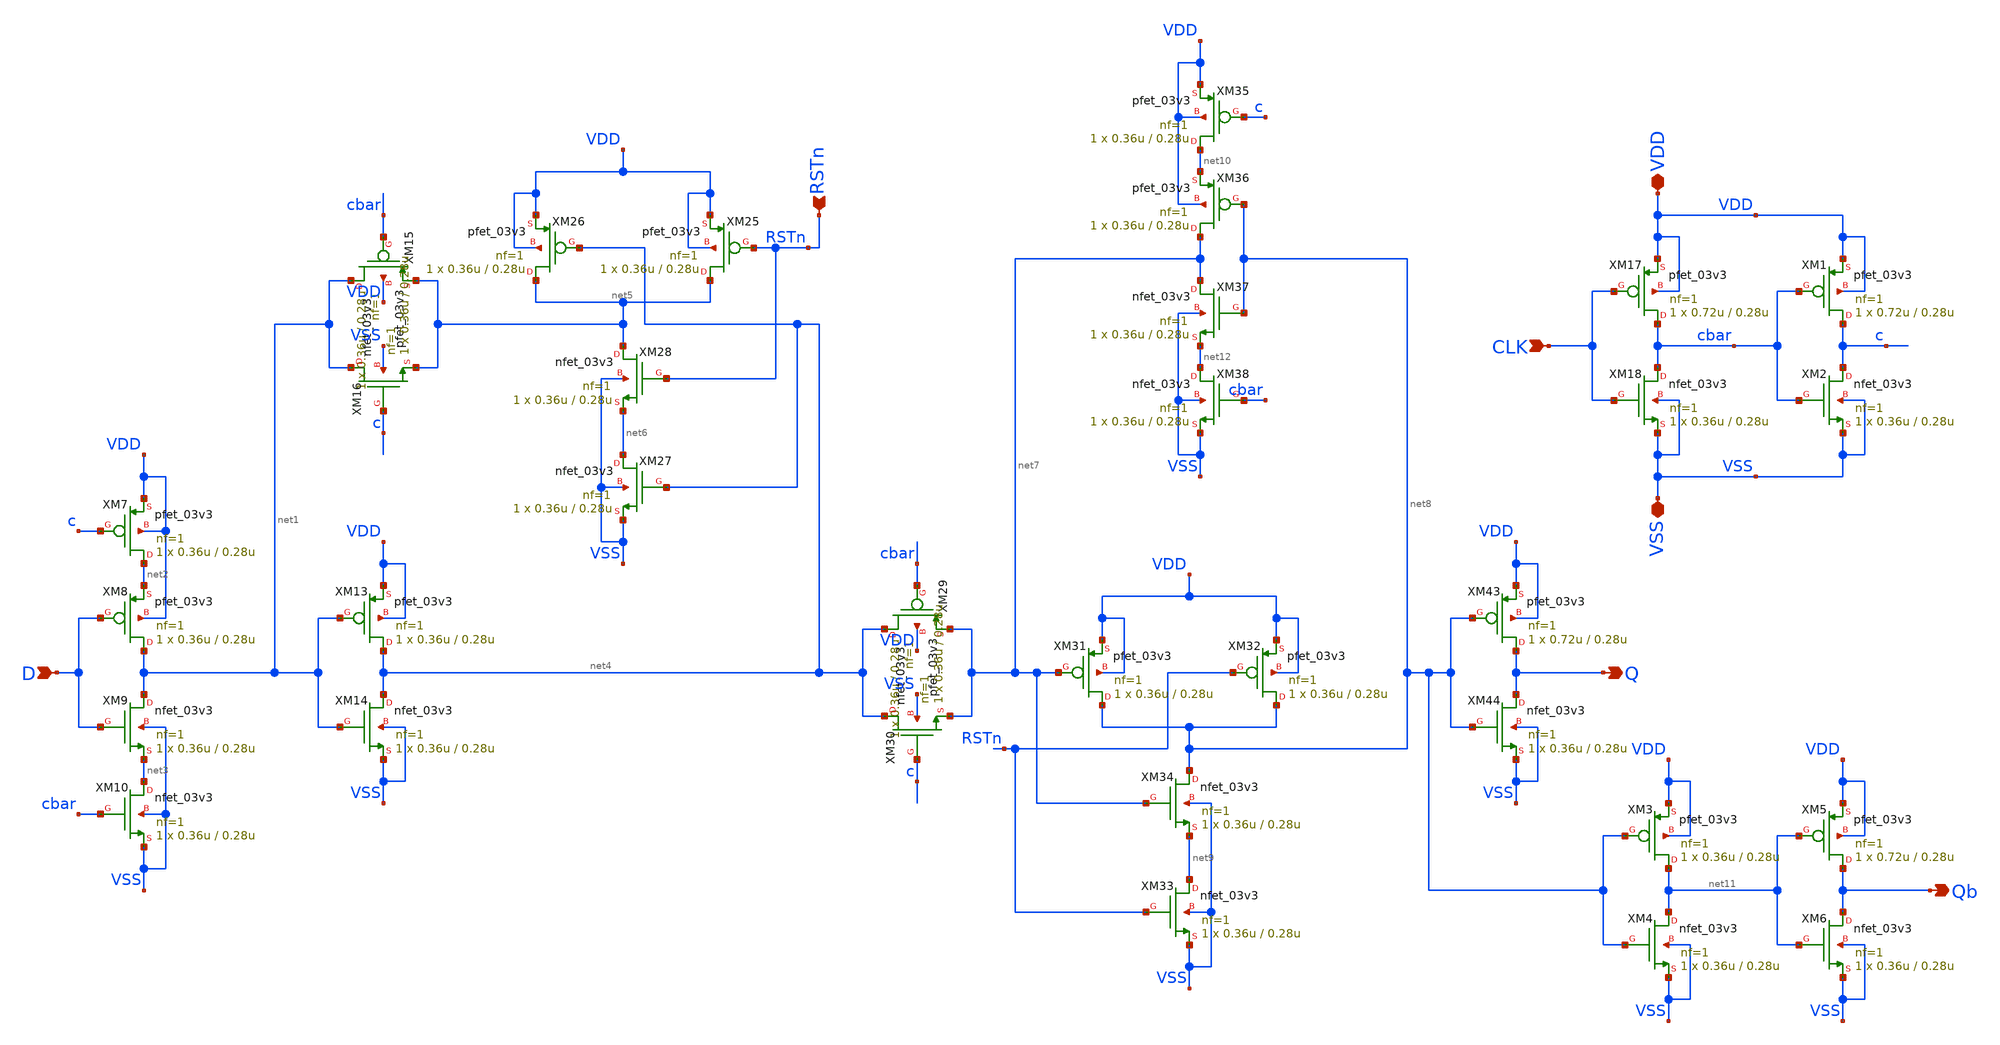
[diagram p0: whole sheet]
** sch_path: CAD6/cad2_dff.sch
**.subckt cad2_dff D CLK Q VDD VSS RSTn Qb
*.ipin D
*.ipin CLK
*.opin Q
*.iopin VDD
*.iopin VSS
*.ipin RSTn
*.opin Qb
XM7 net2 c VDD VDD pfet_03v3 L=0.28u W=0.36u nf=1 ad='int((nf+1)/2) * W/nf * 0.18u' as='int((nf+2)/2) * W/nf * 0.18u'
+ pd='2*int((nf+1)/2) * (W/nf + 0.18u)' ps='2*int((nf+2)/2) * (W/nf + 0.18u)' nrd='0.18u / W' nrs='0.18u / W'
+ sa=0 sb=0 sd=0 m=1
XM8 net1 D net2 VDD pfet_03v3 L=0.28u W=0.36u nf=1 ad='int((nf+1)/2) * W/nf * 0.18u' as='int((nf+2)/2) * W/nf * 0.18u'
+ pd='2*int((nf+1)/2) * (W/nf + 0.18u)' ps='2*int((nf+2)/2) * (W/nf + 0.18u)' nrd='0.18u / W' nrs='0.18u / W'
+ sa=0 sb=0 sd=0 m=1
XM9 net1 D net3 VSS nfet_03v3 L=0.28u W=0.36u nf=1 ad='int((nf+1)/2) * W/nf * 0.18u' as='int((nf+2)/2) * W/nf * 0.18u'
+ pd='2*int((nf+1)/2) * (W/nf + 0.18u)' ps='2*int((nf+2)/2) * (W/nf + 0.18u)' nrd='0.18u / W' nrs='0.18u / W'
+ sa=0 sb=0 sd=0 m=1
XM10 net3 cbar VSS VSS nfet_03v3 L=0.28u W=0.36u nf=1 ad='int((nf+1)/2) * W/nf * 0.18u' as='int((nf+2)/2) * W/nf * 0.18u'
+ pd='2*int((nf+1)/2) * (W/nf + 0.18u)' ps='2*int((nf+2)/2) * (W/nf + 0.18u)' nrd='0.18u / W' nrs='0.18u / W'
+ sa=0 sb=0 sd=0 m=1
XM13 net4 net1 VDD VDD pfet_03v3 L=0.28u W=0.36u nf=1 ad='int((nf+1)/2) * W/nf * 0.18u' as='int((nf+2)/2) * W/nf * 0.18u'
+ pd='2*int((nf+1)/2) * (W/nf + 0.18u)' ps='2*int((nf+2)/2) * (W/nf + 0.18u)' nrd='0.18u / W' nrs='0.18u / W'
+ sa=0 sb=0 sd=0 m=1
XM14 net4 net1 VSS VSS nfet_03v3 L=0.28u W=0.36u nf=1 ad='int((nf+1)/2) * W/nf * 0.18u' as='int((nf+2)/2) * W/nf * 0.18u'
+ pd='2*int((nf+1)/2) * (W/nf + 0.18u)' ps='2*int((nf+2)/2) * (W/nf + 0.18u)' nrd='0.18u / W' nrs='0.18u / W'
+ sa=0 sb=0 sd=0 m=1
XM15 net1 cbar net5 VDD pfet_03v3 L=0.28u W=0.36u nf=1 ad='int((nf+1)/2) * W/nf * 0.18u' as='int((nf+2)/2) * W/nf * 0.18u'
+ pd='2*int((nf+1)/2) * (W/nf + 0.18u)' ps='2*int((nf+2)/2) * (W/nf + 0.18u)' nrd='0.18u / W' nrs='0.18u / W'
+ sa=0 sb=0 sd=0 m=1
XM16 net1 c net5 VSS nfet_03v3 L=0.28u W=0.36u nf=1 ad='int((nf+1)/2) * W/nf * 0.18u' as='int((nf+2)/2) * W/nf * 0.18u'
+ pd='2*int((nf+1)/2) * (W/nf + 0.18u)' ps='2*int((nf+2)/2) * (W/nf + 0.18u)' nrd='0.18u / W' nrs='0.18u / W'
+ sa=0 sb=0 sd=0 m=1
XM17 cbar CLK VDD VDD pfet_03v3 L=0.28u W=0.72u nf=1 ad='int((nf+1)/2) * W/nf * 0.18u' as='int((nf+2)/2) * W/nf * 0.18u'
+ pd='2*int((nf+1)/2) * (W/nf + 0.18u)' ps='2*int((nf+2)/2) * (W/nf + 0.18u)' nrd='0.18u / W' nrs='0.18u / W'
+ sa=0 sb=0 sd=0 m=1
XM18 cbar CLK VSS VSS nfet_03v3 L=0.28u W=0.36u nf=1 ad='int((nf+1)/2) * W/nf * 0.18u' as='int((nf+2)/2) * W/nf * 0.18u'
+ pd='2*int((nf+1)/2) * (W/nf + 0.18u)' ps='2*int((nf+2)/2) * (W/nf + 0.18u)' nrd='0.18u / W' nrs='0.18u / W'
+ sa=0 sb=0 sd=0 m=1
XM25 net5 RSTn VDD VDD pfet_03v3 L=0.28u W=0.36u nf=1 ad='int((nf+1)/2) * W/nf * 0.18u' as='int((nf+2)/2) * W/nf * 0.18u'
+ pd='2*int((nf+1)/2) * (W/nf + 0.18u)' ps='2*int((nf+2)/2) * (W/nf + 0.18u)' nrd='0.18u / W' nrs='0.18u / W'
+ sa=0 sb=0 sd=0 m=1
XM26 net5 net4 VDD VDD pfet_03v3 L=0.28u W=0.36u nf=1 ad='int((nf+1)/2) * W/nf * 0.18u' as='int((nf+2)/2) * W/nf * 0.18u'
+ pd='2*int((nf+1)/2) * (W/nf + 0.18u)' ps='2*int((nf+2)/2) * (W/nf + 0.18u)' nrd='0.18u / W' nrs='0.18u / W'
+ sa=0 sb=0 sd=0 m=1
XM27 net6 net4 VSS VSS nfet_03v3 L=0.28u W=0.36u nf=1 ad='int((nf+1)/2) * W/nf * 0.18u' as='int((nf+2)/2) * W/nf * 0.18u'
+ pd='2*int((nf+1)/2) * (W/nf + 0.18u)' ps='2*int((nf+2)/2) * (W/nf + 0.18u)' nrd='0.18u / W' nrs='0.18u / W'
+ sa=0 sb=0 sd=0 m=1
XM28 net5 RSTn net6 VSS nfet_03v3 L=0.28u W=0.36u nf=1 ad='int((nf+1)/2) * W/nf * 0.18u' as='int((nf+2)/2) * W/nf * 0.18u'
+ pd='2*int((nf+1)/2) * (W/nf + 0.18u)' ps='2*int((nf+2)/2) * (W/nf + 0.18u)' nrd='0.18u / W' nrs='0.18u / W'
+ sa=0 sb=0 sd=0 m=1
XM29 net4 cbar net7 VDD pfet_03v3 L=0.28u W=0.36u nf=1 ad='int((nf+1)/2) * W/nf * 0.18u' as='int((nf+2)/2) * W/nf * 0.18u'
+ pd='2*int((nf+1)/2) * (W/nf + 0.18u)' ps='2*int((nf+2)/2) * (W/nf + 0.18u)' nrd='0.18u / W' nrs='0.18u / W'
+ sa=0 sb=0 sd=0 m=1
XM30 net4 c net7 VSS nfet_03v3 L=0.28u W=0.36u nf=1 ad='int((nf+1)/2) * W/nf * 0.18u' as='int((nf+2)/2) * W/nf * 0.18u'
+ pd='2*int((nf+1)/2) * (W/nf + 0.18u)' ps='2*int((nf+2)/2) * (W/nf + 0.18u)' nrd='0.18u / W' nrs='0.18u / W'
+ sa=0 sb=0 sd=0 m=1
XM31 net8 net7 VDD VDD pfet_03v3 L=0.28u W=0.36u nf=1 ad='int((nf+1)/2) * W/nf * 0.18u' as='int((nf+2)/2) * W/nf * 0.18u'
+ pd='2*int((nf+1)/2) * (W/nf + 0.18u)' ps='2*int((nf+2)/2) * (W/nf + 0.18u)' nrd='0.18u / W' nrs='0.18u / W'
+ sa=0 sb=0 sd=0 m=1
XM32 net8 RSTn VDD VDD pfet_03v3 L=0.28u W=0.36u nf=1 ad='int((nf+1)/2) * W/nf * 0.18u' as='int((nf+2)/2) * W/nf * 0.18u'
+ pd='2*int((nf+1)/2) * (W/nf + 0.18u)' ps='2*int((nf+2)/2) * (W/nf + 0.18u)' nrd='0.18u / W' nrs='0.18u / W'
+ sa=0 sb=0 sd=0 m=1
XM33 net9 RSTn VSS VSS nfet_03v3 L=0.28u W=0.36u nf=1 ad='int((nf+1)/2) * W/nf * 0.18u' as='int((nf+2)/2) * W/nf * 0.18u'
+ pd='2*int((nf+1)/2) * (W/nf + 0.18u)' ps='2*int((nf+2)/2) * (W/nf + 0.18u)' nrd='0.18u / W' nrs='0.18u / W'
+ sa=0 sb=0 sd=0 m=1
XM34 net8 net7 net9 VSS nfet_03v3 L=0.28u W=0.36u nf=1 ad='int((nf+1)/2) * W/nf * 0.18u' as='int((nf+2)/2) * W/nf * 0.18u'
+ pd='2*int((nf+1)/2) * (W/nf + 0.18u)' ps='2*int((nf+2)/2) * (W/nf + 0.18u)' nrd='0.18u / W' nrs='0.18u / W'
+ sa=0 sb=0 sd=0 m=1
XM35 net10 c VDD VDD pfet_03v3 L=0.28u W=0.36u nf=1 ad='int((nf+1)/2) * W/nf * 0.18u' as='int((nf+2)/2) * W/nf * 0.18u'
+ pd='2*int((nf+1)/2) * (W/nf + 0.18u)' ps='2*int((nf+2)/2) * (W/nf + 0.18u)' nrd='0.18u / W' nrs='0.18u / W'
+ sa=0 sb=0 sd=0 m=1
XM36 net7 net8 net10 VDD pfet_03v3 L=0.28u W=0.36u nf=1 ad='int((nf+1)/2) * W/nf * 0.18u' as='int((nf+2)/2) * W/nf * 0.18u'
+ pd='2*int((nf+1)/2) * (W/nf + 0.18u)' ps='2*int((nf+2)/2) * (W/nf + 0.18u)' nrd='0.18u / W' nrs='0.18u / W'
+ sa=0 sb=0 sd=0 m=1
XM37 net7 net8 net12 VSS nfet_03v3 L=0.28u W=0.36u nf=1 ad='int((nf+1)/2) * W/nf * 0.18u' as='int((nf+2)/2) * W/nf * 0.18u'
+ pd='2*int((nf+1)/2) * (W/nf + 0.18u)' ps='2*int((nf+2)/2) * (W/nf + 0.18u)' nrd='0.18u / W' nrs='0.18u / W'
+ sa=0 sb=0 sd=0 m=1
XM38 net12 cbar VSS VSS nfet_03v3 L=0.28u W=0.36u nf=1 ad='int((nf+1)/2) * W/nf * 0.18u' as='int((nf+2)/2) * W/nf * 0.18u'
+ pd='2*int((nf+1)/2) * (W/nf + 0.18u)' ps='2*int((nf+2)/2) * (W/nf + 0.18u)' nrd='0.18u / W' nrs='0.18u / W'
+ sa=0 sb=0 sd=0 m=1
XM43 Q net8 VDD VDD pfet_03v3 L=0.28u W=0.72u nf=1 ad='int((nf+1)/2) * W/nf * 0.18u' as='int((nf+2)/2) * W/nf * 0.18u'
+ pd='2*int((nf+1)/2) * (W/nf + 0.18u)' ps='2*int((nf+2)/2) * (W/nf + 0.18u)' nrd='0.18u / W' nrs='0.18u / W'
+ sa=0 sb=0 sd=0 m=1
XM44 Q net8 VSS VSS nfet_03v3 L=0.28u W=0.36u nf=1 ad='int((nf+1)/2) * W/nf * 0.18u' as='int((nf+2)/2) * W/nf * 0.18u'
+ pd='2*int((nf+1)/2) * (W/nf + 0.18u)' ps='2*int((nf+2)/2) * (W/nf + 0.18u)' nrd='0.18u / W' nrs='0.18u / W'
+ sa=0 sb=0 sd=0 m=1
XM1 c cbar VDD VDD pfet_03v3 L=0.28u W=0.72u nf=1 ad='int((nf+1)/2) * W/nf * 0.18u' as='int((nf+2)/2) * W/nf * 0.18u'
+ pd='2*int((nf+1)/2) * (W/nf + 0.18u)' ps='2*int((nf+2)/2) * (W/nf + 0.18u)' nrd='0.18u / W' nrs='0.18u / W'
+ sa=0 sb=0 sd=0 m=1
XM2 c cbar VSS VSS nfet_03v3 L=0.28u W=0.36u nf=1 ad='int((nf+1)/2) * W/nf * 0.18u' as='int((nf+2)/2) * W/nf * 0.18u'
+ pd='2*int((nf+1)/2) * (W/nf + 0.18u)' ps='2*int((nf+2)/2) * (W/nf + 0.18u)' nrd='0.18u / W' nrs='0.18u / W'
+ sa=0 sb=0 sd=0 m=1
XM3 net11 net8 VDD VDD pfet_03v3 L=0.28u W=0.36u nf=1 ad='int((nf+1)/2) * W/nf * 0.18u' as='int((nf+2)/2) * W/nf * 0.18u'
+ pd='2*int((nf+1)/2) * (W/nf + 0.18u)' ps='2*int((nf+2)/2) * (W/nf + 0.18u)' nrd='0.18u / W' nrs='0.18u / W'
+ sa=0 sb=0 sd=0 m=1
XM4 net11 net8 VSS VSS nfet_03v3 L=0.28u W=0.36u nf=1 ad='int((nf+1)/2) * W/nf * 0.18u' as='int((nf+2)/2) * W/nf * 0.18u'
+ pd='2*int((nf+1)/2) * (W/nf + 0.18u)' ps='2*int((nf+2)/2) * (W/nf + 0.18u)' nrd='0.18u / W' nrs='0.18u / W'
+ sa=0 sb=0 sd=0 m=1
XM5 Qb net11 VDD VDD pfet_03v3 L=0.28u W=0.72u nf=1 ad='int((nf+1)/2) * W/nf * 0.18u' as='int((nf+2)/2) * W/nf * 0.18u'
+ pd='2*int((nf+1)/2) * (W/nf + 0.18u)' ps='2*int((nf+2)/2) * (W/nf + 0.18u)' nrd='0.18u / W' nrs='0.18u / W'
+ sa=0 sb=0 sd=0 m=1
XM6 Qb net11 VSS VSS nfet_03v3 L=0.28u W=0.36u nf=1 ad='int((nf+1)/2) * W/nf * 0.18u' as='int((nf+2)/2) * W/nf * 0.18u'
+ pd='2*int((nf+1)/2) * (W/nf + 0.18u)' ps='2*int((nf+2)/2) * (W/nf + 0.18u)' nrd='0.18u / W' nrs='0.18u / W'
+ sa=0 sb=0 sd=0 m=1
**.ends
.end
